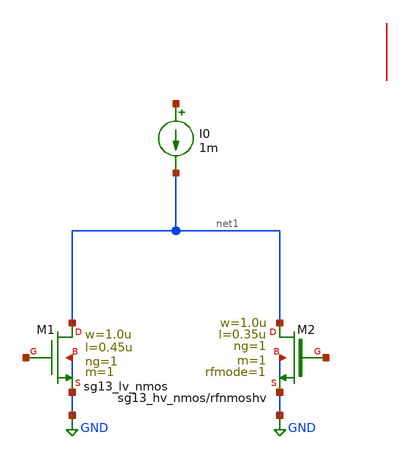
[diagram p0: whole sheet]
** sch_path: CKT_6/xschem/circuit.sch
* Copyright 2023 IHP PDK Authors
* Licensed under the Apache License, Version 2.0 (the "License");
* you may not use this file except in compliance with the License.
* You may obtain a copy of the License at
* https://www.apache.org/licenses/LICENSE-2.0
* Unless required by applicable law or agreed to in writing, software
* distributed under the License is distributed on an "AS IS" BASIS,
* WITHOUT WARRANTIES OR CONDITIONS OF ANY KIND, either express or implied.
* See the License for the specific language governing permissions and
* limitations under the License.
**.subckt circuit
XM1 net1 net2 GND GND sg13_lv_nmos w=1.0u l=0.45u ng=1 m=1 mm_ok=1
XM2 net1 net3 GND GND sg13_hv_nmos w=1.0u l=0.35u ng=1 m=1 rfmode=1 mm_ok=1
I0 net4 net1 1m
**.ends
.GLOBAL GND
.end
